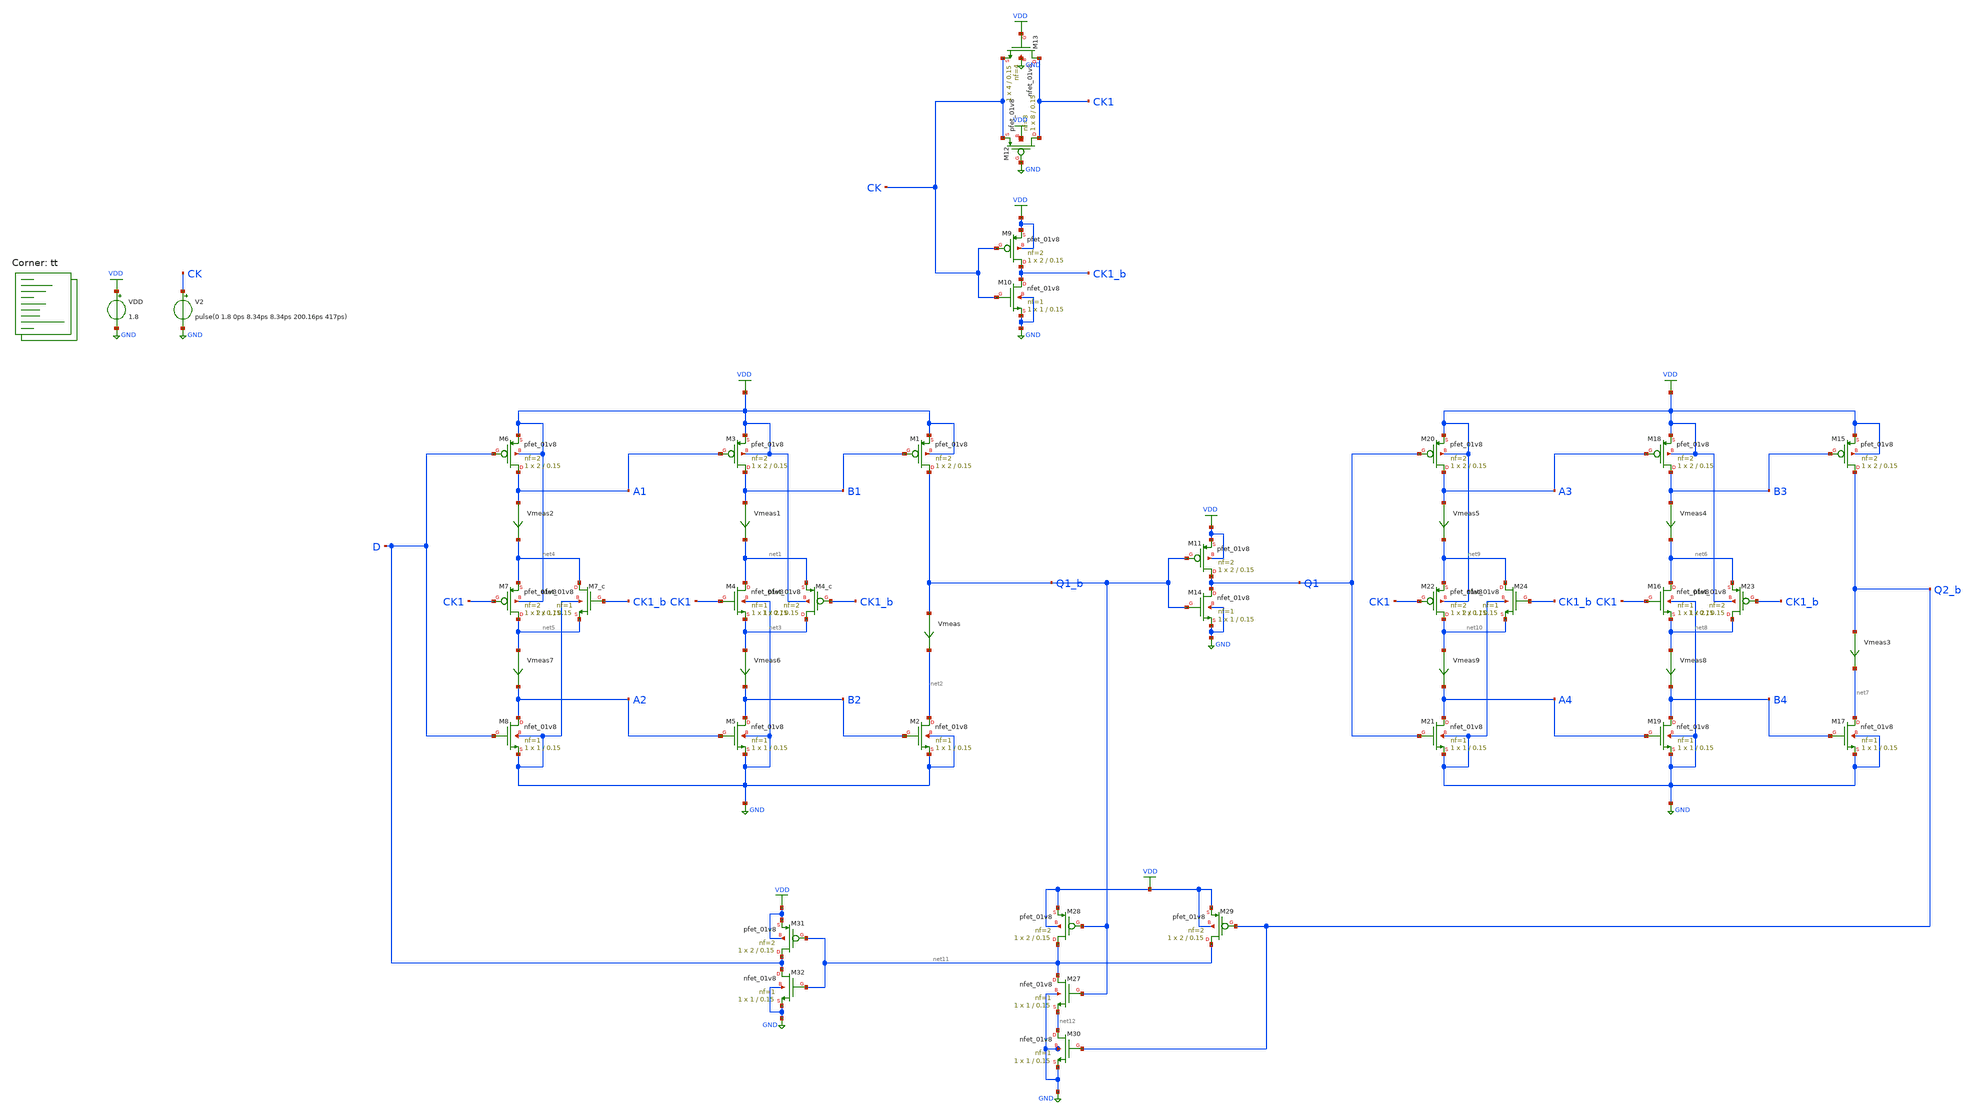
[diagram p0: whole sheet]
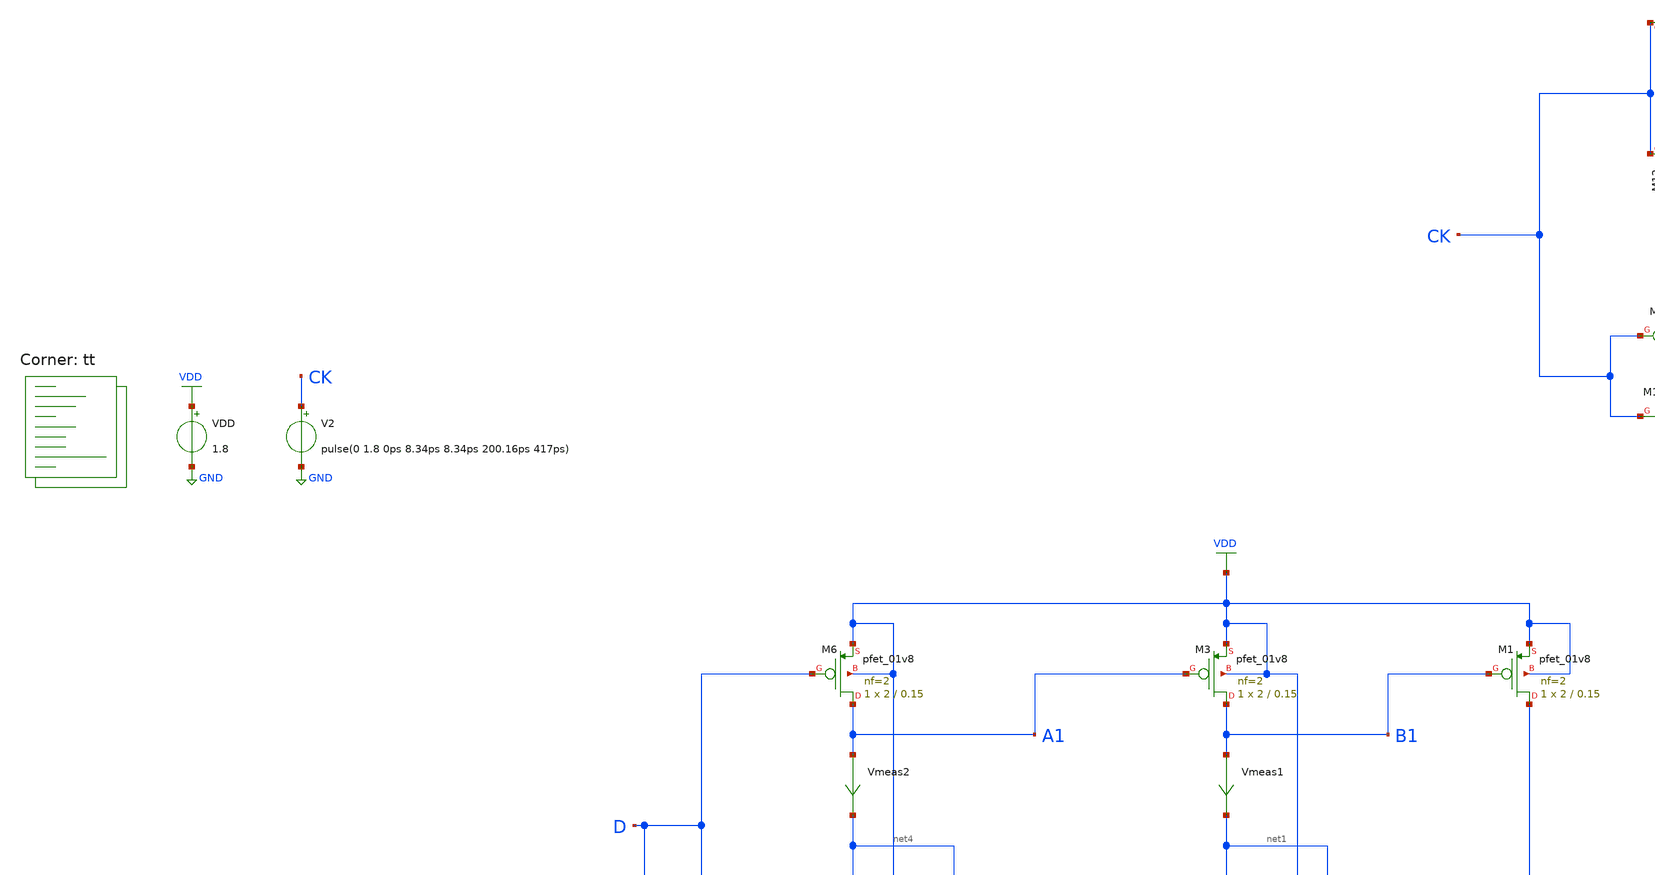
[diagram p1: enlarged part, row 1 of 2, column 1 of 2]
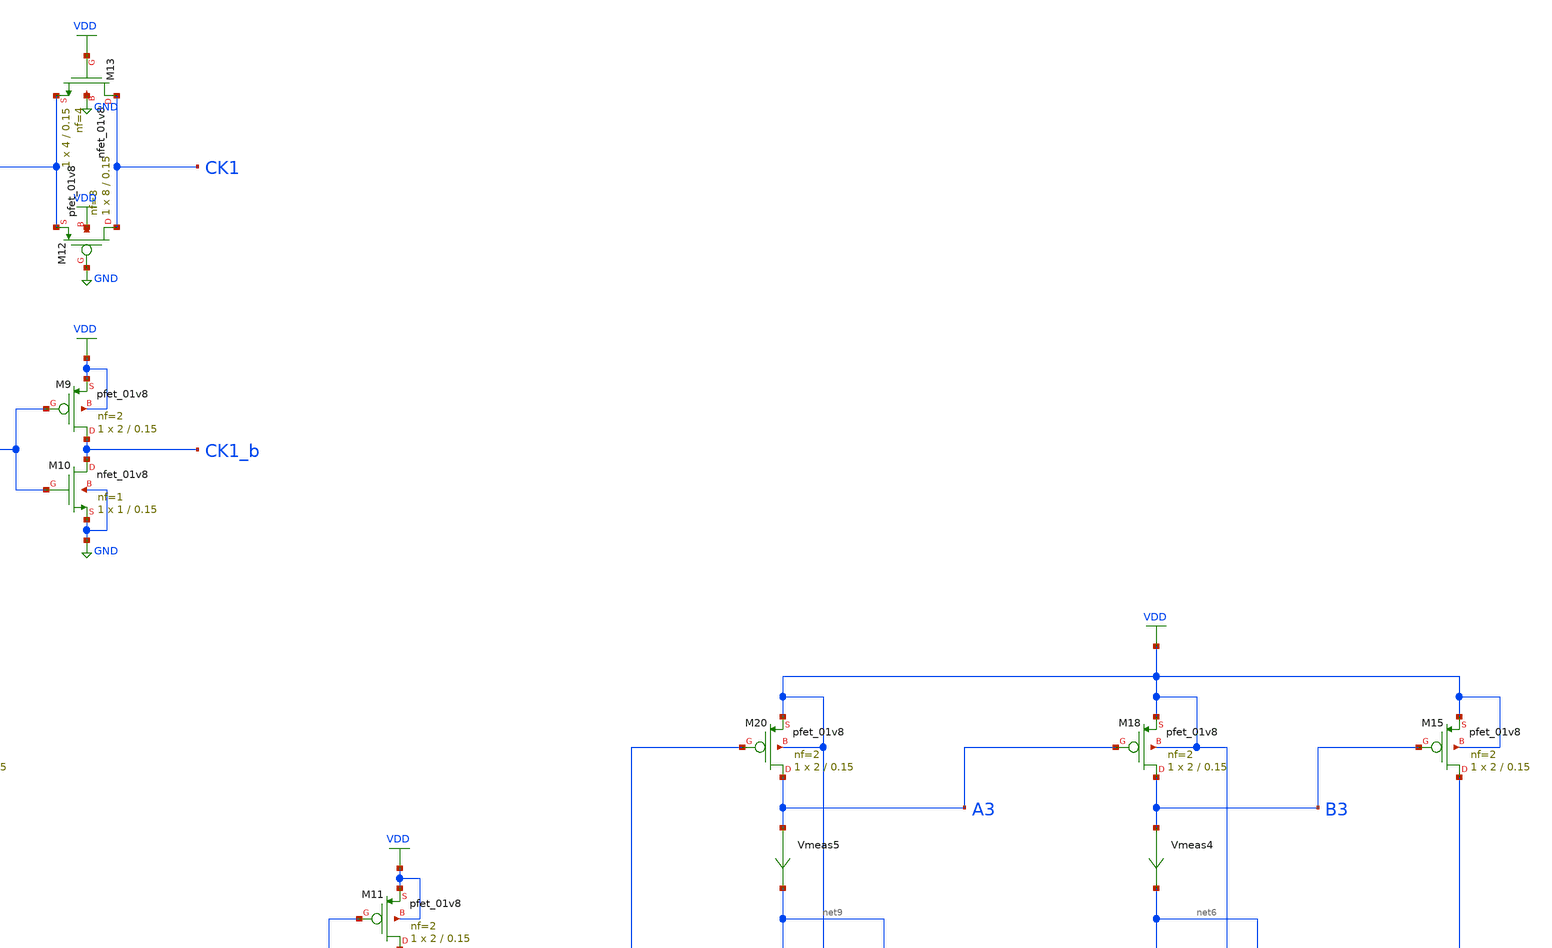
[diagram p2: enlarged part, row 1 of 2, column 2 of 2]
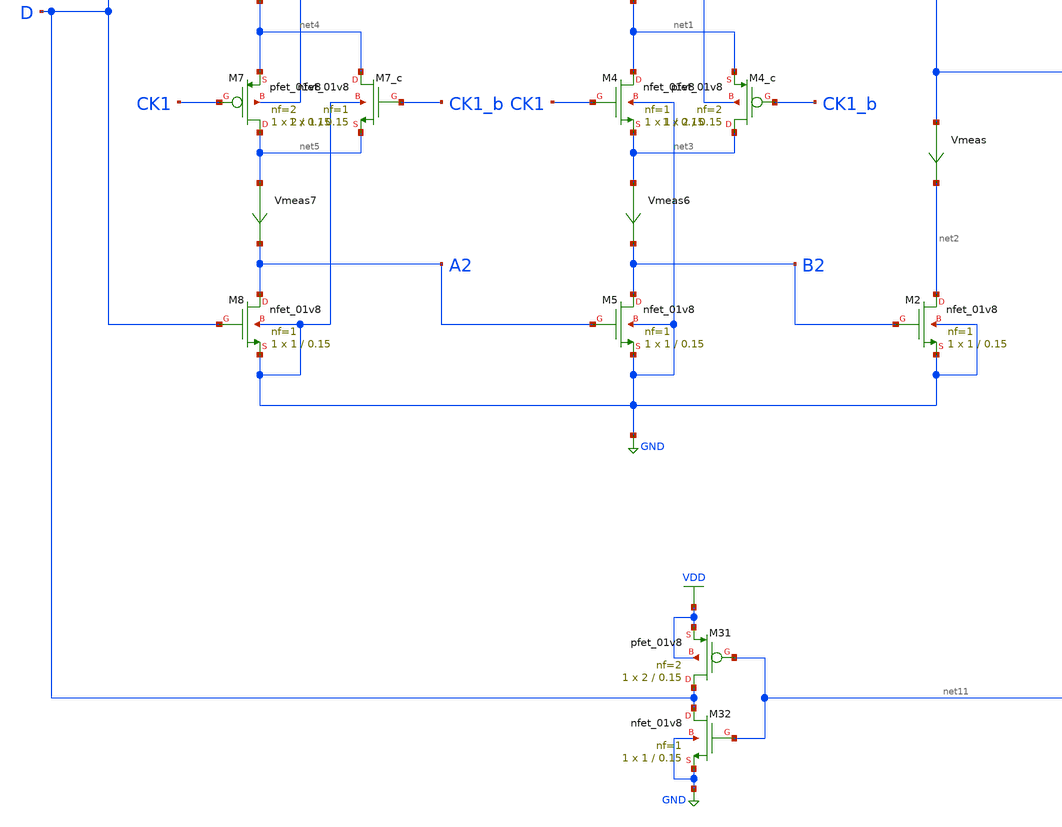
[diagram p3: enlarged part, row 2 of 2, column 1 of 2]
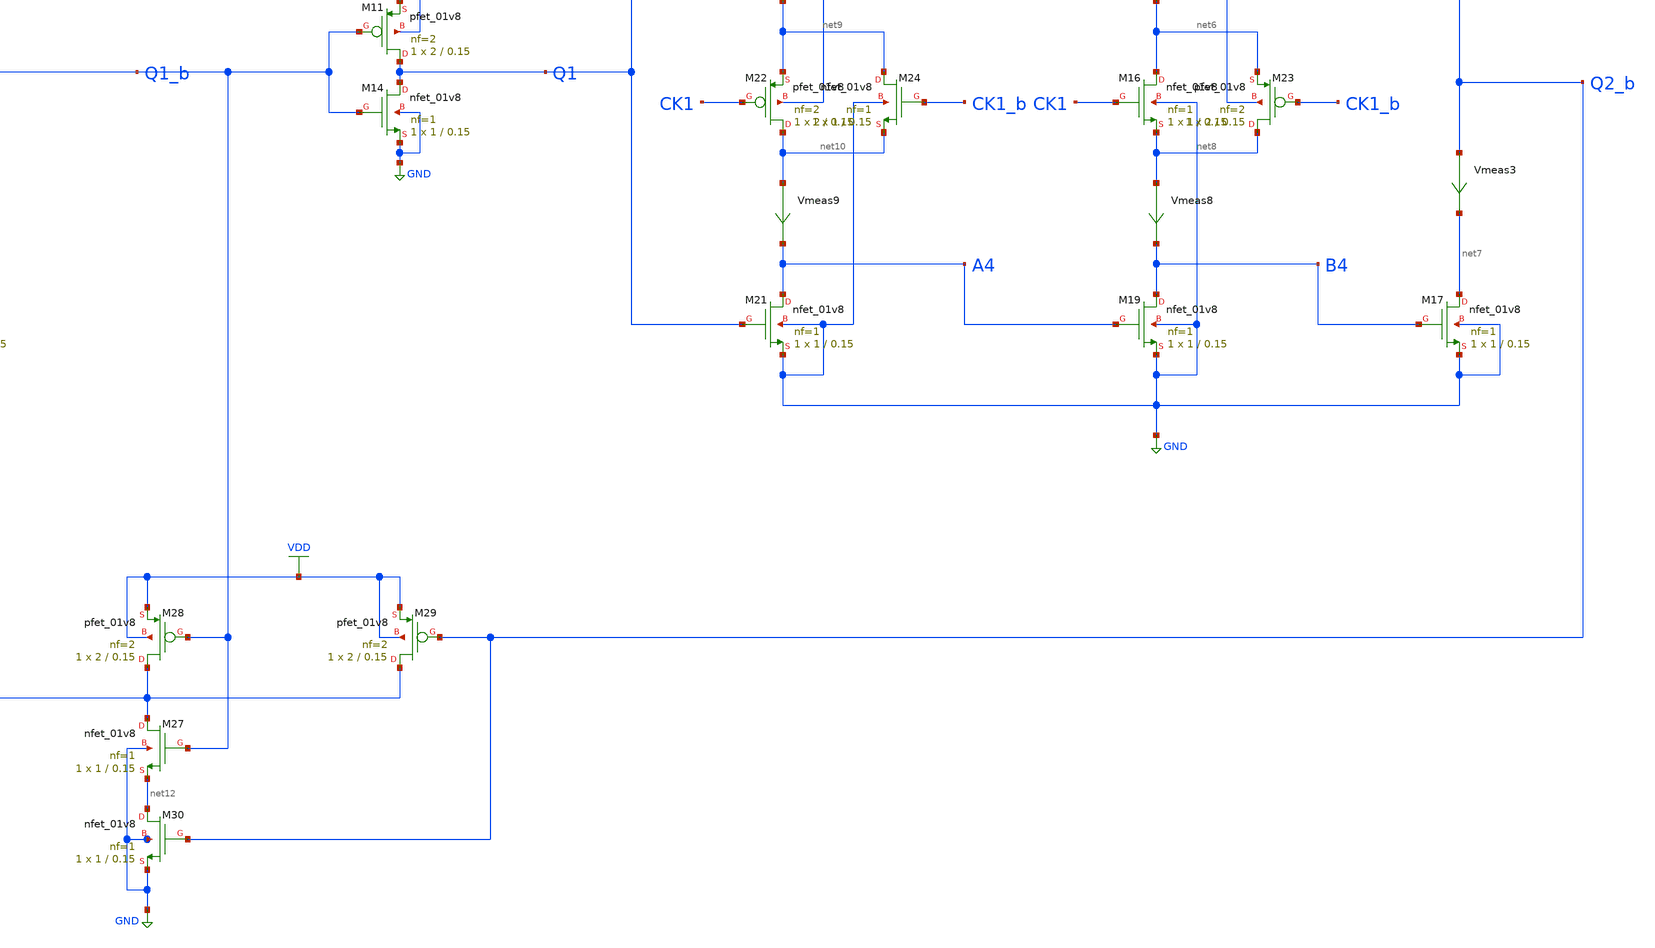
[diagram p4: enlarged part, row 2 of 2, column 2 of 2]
** sch_path: projects/pll/divider/xschem_ngspice/tb_TSPC_FF_comp_sw_divide3.sch
**.subckt tb_TSPC_FF_comp_sw_divide3
VDD VDD GND 1.8
XM1 Q1_b B1 VDD VDD sky130_fd_pr__pfet_01v8 L=0.15 W=2 nf=2 ad='int((nf+1)/2) * W/nf * 0.29' as='int((nf+2)/2) * W/nf * 0.29'
+ pd='2*int((nf+1)/2) * (W/nf + 0.29)' ps='2*int((nf+2)/2) * (W/nf + 0.29)' nrd='0.29 / W' nrs='0.29 / W'
+ sa=0 sb=0 sd=0 mult=1 m=1
XM4 net1 CK1 net3 GND sky130_fd_pr__nfet_01v8 L=0.15 W=1 nf=1 ad='int((nf+1)/2) * W/nf * 0.29' as='int((nf+2)/2) * W/nf * 0.29'
+ pd='2*int((nf+1)/2) * (W/nf + 0.29)' ps='2*int((nf+2)/2) * (W/nf + 0.29)' nrd='0.29 / W' nrs='0.29 / W'
+ sa=0 sb=0 sd=0 mult=1 m=1
Vmeas Q1_b net2 0
.save i(vmeas)
XM2 net2 B2 GND GND sky130_fd_pr__nfet_01v8 L=0.15 W=1 nf=1 ad='int((nf+1)/2) * W/nf * 0.29' as='int((nf+2)/2) * W/nf * 0.29'
+ pd='2*int((nf+1)/2) * (W/nf + 0.29)' ps='2*int((nf+2)/2) * (W/nf + 0.29)' nrd='0.29 / W' nrs='0.29 / W'
+ sa=0 sb=0 sd=0 mult=1 m=1
XM3 B1 A1 VDD VDD sky130_fd_pr__pfet_01v8 L=0.15 W=2 nf=2 ad='int((nf+1)/2) * W/nf * 0.29' as='int((nf+2)/2) * W/nf * 0.29'
+ pd='2*int((nf+1)/2) * (W/nf + 0.29)' ps='2*int((nf+2)/2) * (W/nf + 0.29)' nrd='0.29 / W' nrs='0.29 / W'
+ sa=0 sb=0 sd=0 mult=1 m=1
XM5 B2 A2 GND GND sky130_fd_pr__nfet_01v8 L=0.15 W=1 nf=1 ad='int((nf+1)/2) * W/nf * 0.29' as='int((nf+2)/2) * W/nf * 0.29'
+ pd='2*int((nf+1)/2) * (W/nf + 0.29)' ps='2*int((nf+2)/2) * (W/nf + 0.29)' nrd='0.29 / W' nrs='0.29 / W'
+ sa=0 sb=0 sd=0 mult=1 m=1
Vmeas1 B1 net1 0
.save i(vmeas1)
XM6 A1 D VDD VDD sky130_fd_pr__pfet_01v8 L=0.15 W=2 nf=2 ad='int((nf+1)/2) * W/nf * 0.29' as='int((nf+2)/2) * W/nf * 0.29'
+ pd='2*int((nf+1)/2) * (W/nf + 0.29)' ps='2*int((nf+2)/2) * (W/nf + 0.29)' nrd='0.29 / W' nrs='0.29 / W'
+ sa=0 sb=0 sd=0 mult=1 m=1
XM8 A2 D GND GND sky130_fd_pr__nfet_01v8 L=0.15 W=1 nf=1 ad='int((nf+1)/2) * W/nf * 0.29' as='int((nf+2)/2) * W/nf * 0.29'
+ pd='2*int((nf+1)/2) * (W/nf + 0.29)' ps='2*int((nf+2)/2) * (W/nf + 0.29)' nrd='0.29 / W' nrs='0.29 / W'
+ sa=0 sb=0 sd=0 mult=1 m=1
Vmeas2 A1 net4 0
.save i(vmeas2)
XM7 net5 CK1 net4 VDD sky130_fd_pr__pfet_01v8 L=0.15 W=2 nf=2 ad='int((nf+1)/2) * W/nf * 0.29' as='int((nf+2)/2) * W/nf * 0.29'
+ pd='2*int((nf+1)/2) * (W/nf + 0.29)' ps='2*int((nf+2)/2) * (W/nf + 0.29)' nrd='0.29 / W' nrs='0.29 / W'
+ sa=0 sb=0 sd=0 mult=1 m=1
XM4_c net3 CK1_b net1 VDD sky130_fd_pr__pfet_01v8 L=0.15 W=2 nf=2 ad='int((nf+1)/2) * W/nf * 0.29' as='int((nf+2)/2) * W/nf * 0.29'
+ pd='2*int((nf+1)/2) * (W/nf + 0.29)' ps='2*int((nf+2)/2) * (W/nf + 0.29)' nrd='0.29 / W' nrs='0.29 / W'
+ sa=0 sb=0 sd=0 mult=1 m=1
XM7_c net4 CK1_b net5 GND sky130_fd_pr__nfet_01v8 L=0.15 W=1 nf=1 ad='int((nf+1)/2) * W/nf * 0.29' as='int((nf+2)/2) * W/nf * 0.29'
+ pd='2*int((nf+1)/2) * (W/nf + 0.29)' ps='2*int((nf+2)/2) * (W/nf + 0.29)' nrd='0.29 / W' nrs='0.29 / W'
+ sa=0 sb=0 sd=0 mult=1 m=1
XM12 CK1 GND CK VDD sky130_fd_pr__pfet_01v8 L=0.15 W=8 nf=8 ad='int((nf+1)/2) * W/nf * 0.29' as='int((nf+2)/2) * W/nf * 0.29'
+ pd='2*int((nf+1)/2) * (W/nf + 0.29)' ps='2*int((nf+2)/2) * (W/nf + 0.29)' nrd='0.29 / W' nrs='0.29 / W'
+ sa=0 sb=0 sd=0 mult=1 m=1
XM13 CK1 VDD CK GND sky130_fd_pr__nfet_01v8 L=0.15 W=4 nf=4 ad='int((nf+1)/2) * W/nf * 0.29' as='int((nf+2)/2) * W/nf * 0.29'
+ pd='2*int((nf+1)/2) * (W/nf + 0.29)' ps='2*int((nf+2)/2) * (W/nf + 0.29)' nrd='0.29 / W' nrs='0.29 / W'
+ sa=0 sb=0 sd=0 mult=1 m=1
XM9 CK1_b CK VDD VDD sky130_fd_pr__pfet_01v8 L=0.15 W=2 nf=2 ad='int((nf+1)/2) * W/nf * 0.29' as='int((nf+2)/2) * W/nf * 0.29'
+ pd='2*int((nf+1)/2) * (W/nf + 0.29)' ps='2*int((nf+2)/2) * (W/nf + 0.29)' nrd='0.29 / W' nrs='0.29 / W'
+ sa=0 sb=0 sd=0 mult=1 m=1
XM10 CK1_b CK GND GND sky130_fd_pr__nfet_01v8 L=0.15 W=1 nf=1 ad='int((nf+1)/2) * W/nf * 0.29' as='int((nf+2)/2) * W/nf * 0.29'
+ pd='2*int((nf+1)/2) * (W/nf + 0.29)' ps='2*int((nf+2)/2) * (W/nf + 0.29)' nrd='0.29 / W' nrs='0.29 / W'
+ sa=0 sb=0 sd=0 mult=1 m=1
XM15 Q2_b B3 VDD VDD sky130_fd_pr__pfet_01v8 L=0.15 W=2 nf=2 ad='int((nf+1)/2) * W/nf * 0.29' as='int((nf+2)/2) * W/nf * 0.29'
+ pd='2*int((nf+1)/2) * (W/nf + 0.29)' ps='2*int((nf+2)/2) * (W/nf + 0.29)' nrd='0.29 / W' nrs='0.29 / W'
+ sa=0 sb=0 sd=0 mult=1 m=1
XM16 net6 CK1 net8 GND sky130_fd_pr__nfet_01v8 L=0.15 W=1 nf=1 ad='int((nf+1)/2) * W/nf * 0.29' as='int((nf+2)/2) * W/nf * 0.29'
+ pd='2*int((nf+1)/2) * (W/nf + 0.29)' ps='2*int((nf+2)/2) * (W/nf + 0.29)' nrd='0.29 / W' nrs='0.29 / W'
+ sa=0 sb=0 sd=0 mult=1 m=1
Vmeas3 Q2_b net7 0
.save i(vmeas3)
XM17 net7 B4 GND GND sky130_fd_pr__nfet_01v8 L=0.15 W=1 nf=1 ad='int((nf+1)/2) * W/nf * 0.29' as='int((nf+2)/2) * W/nf * 0.29'
+ pd='2*int((nf+1)/2) * (W/nf + 0.29)' ps='2*int((nf+2)/2) * (W/nf + 0.29)' nrd='0.29 / W' nrs='0.29 / W'
+ sa=0 sb=0 sd=0 mult=1 m=1
XM18 B3 A3 VDD VDD sky130_fd_pr__pfet_01v8 L=0.15 W=2 nf=2 ad='int((nf+1)/2) * W/nf * 0.29' as='int((nf+2)/2) * W/nf * 0.29'
+ pd='2*int((nf+1)/2) * (W/nf + 0.29)' ps='2*int((nf+2)/2) * (W/nf + 0.29)' nrd='0.29 / W' nrs='0.29 / W'
+ sa=0 sb=0 sd=0 mult=1 m=1
XM19 B4 A4 GND GND sky130_fd_pr__nfet_01v8 L=0.15 W=1 nf=1 ad='int((nf+1)/2) * W/nf * 0.29' as='int((nf+2)/2) * W/nf * 0.29'
+ pd='2*int((nf+1)/2) * (W/nf + 0.29)' ps='2*int((nf+2)/2) * (W/nf + 0.29)' nrd='0.29 / W' nrs='0.29 / W'
+ sa=0 sb=0 sd=0 mult=1 m=1
Vmeas4 B3 net6 0
.save i(vmeas4)
XM20 A3 Q1 VDD VDD sky130_fd_pr__pfet_01v8 L=0.15 W=2 nf=2 ad='int((nf+1)/2) * W/nf * 0.29' as='int((nf+2)/2) * W/nf * 0.29'
+ pd='2*int((nf+1)/2) * (W/nf + 0.29)' ps='2*int((nf+2)/2) * (W/nf + 0.29)' nrd='0.29 / W' nrs='0.29 / W'
+ sa=0 sb=0 sd=0 mult=1 m=1
XM21 A4 Q1 GND GND sky130_fd_pr__nfet_01v8 L=0.15 W=1 nf=1 ad='int((nf+1)/2) * W/nf * 0.29' as='int((nf+2)/2) * W/nf * 0.29'
+ pd='2*int((nf+1)/2) * (W/nf + 0.29)' ps='2*int((nf+2)/2) * (W/nf + 0.29)' nrd='0.29 / W' nrs='0.29 / W'
+ sa=0 sb=0 sd=0 mult=1 m=1
Vmeas5 A3 net9 0
.save i(vmeas5)
XM22 net10 CK1 net9 VDD sky130_fd_pr__pfet_01v8 L=0.15 W=2 nf=2 ad='int((nf+1)/2) * W/nf * 0.29' as='int((nf+2)/2) * W/nf * 0.29'
+ pd='2*int((nf+1)/2) * (W/nf + 0.29)' ps='2*int((nf+2)/2) * (W/nf + 0.29)' nrd='0.29 / W' nrs='0.29 / W'
+ sa=0 sb=0 sd=0 mult=1 m=1
XM23 net8 CK1_b net6 VDD sky130_fd_pr__pfet_01v8 L=0.15 W=2 nf=2 ad='int((nf+1)/2) * W/nf * 0.29' as='int((nf+2)/2) * W/nf * 0.29'
+ pd='2*int((nf+1)/2) * (W/nf + 0.29)' ps='2*int((nf+2)/2) * (W/nf + 0.29)' nrd='0.29 / W' nrs='0.29 / W'
+ sa=0 sb=0 sd=0 mult=1 m=1
XM24 net9 CK1_b net10 GND sky130_fd_pr__nfet_01v8 L=0.15 W=1 nf=1 ad='int((nf+1)/2) * W/nf * 0.29' as='int((nf+2)/2) * W/nf * 0.29'
+ pd='2*int((nf+1)/2) * (W/nf + 0.29)' ps='2*int((nf+2)/2) * (W/nf + 0.29)' nrd='0.29 / W' nrs='0.29 / W'
+ sa=0 sb=0 sd=0 mult=1 m=1
Vmeas6 net3 B2 0
.save i(vmeas6)
Vmeas7 net5 A2 0
.save i(vmeas7)
Vmeas8 net8 B4 0
.save i(vmeas8)
Vmeas9 net10 A4 0
.save i(vmeas9)
V2 CK GND pulse(0 1.8 0ps 8.34ps 8.34ps 200.16ps 417ps)
XM11 Q1 Q1_b VDD VDD sky130_fd_pr__pfet_01v8 L=0.15 W=2 nf=2 ad='int((nf+1)/2) * W/nf * 0.29' as='int((nf+2)/2) * W/nf * 0.29'
+ pd='2*int((nf+1)/2) * (W/nf + 0.29)' ps='2*int((nf+2)/2) * (W/nf + 0.29)' nrd='0.29 / W' nrs='0.29 / W'
+ sa=0 sb=0 sd=0 mult=1 m=1
XM14 Q1 Q1_b GND GND sky130_fd_pr__nfet_01v8 L=0.15 W=1 nf=1 ad='int((nf+1)/2) * W/nf * 0.29' as='int((nf+2)/2) * W/nf * 0.29'
+ pd='2*int((nf+1)/2) * (W/nf + 0.29)' ps='2*int((nf+2)/2) * (W/nf + 0.29)' nrd='0.29 / W' nrs='0.29 / W'
+ sa=0 sb=0 sd=0 mult=1 m=1
XM27 net11 Q1_b net12 GND sky130_fd_pr__nfet_01v8 L=0.15 W=1 nf=1 ad='int((nf+1)/2) * W/nf * 0.29' as='int((nf+2)/2) * W/nf * 0.29'
+ pd='2*int((nf+1)/2) * (W/nf + 0.29)' ps='2*int((nf+2)/2) * (W/nf + 0.29)' nrd='0.29 / W' nrs='0.29 / W'
+ sa=0 sb=0 sd=0 mult=1 m=1
XM28 net11 Q1_b VDD VDD sky130_fd_pr__pfet_01v8 L=0.15 W=2 nf=2 ad='int((nf+1)/2) * W/nf * 0.29' as='int((nf+2)/2) * W/nf * 0.29'
+ pd='2*int((nf+1)/2) * (W/nf + 0.29)' ps='2*int((nf+2)/2) * (W/nf + 0.29)' nrd='0.29 / W' nrs='0.29 / W'
+ sa=0 sb=0 sd=0 mult=1 m=1
XM29 net11 Q2_b VDD VDD sky130_fd_pr__pfet_01v8 L=0.15 W=2 nf=2 ad='int((nf+1)/2) * W/nf * 0.29' as='int((nf+2)/2) * W/nf * 0.29'
+ pd='2*int((nf+1)/2) * (W/nf + 0.29)' ps='2*int((nf+2)/2) * (W/nf + 0.29)' nrd='0.29 / W' nrs='0.29 / W'
+ sa=0 sb=0 sd=0 mult=1 m=1
XM30 net12 Q2_b GND GND sky130_fd_pr__nfet_01v8 L=0.15 W=1 nf=1 ad='int((nf+1)/2) * W/nf * 0.29' as='int((nf+2)/2) * W/nf * 0.29'
+ pd='2*int((nf+1)/2) * (W/nf + 0.29)' ps='2*int((nf+2)/2) * (W/nf + 0.29)' nrd='0.29 / W' nrs='0.29 / W'
+ sa=0 sb=0 sd=0 mult=1 m=1
XM31 D net11 VDD VDD sky130_fd_pr__pfet_01v8 L=0.15 W=2 nf=2 ad='int((nf+1)/2) * W/nf * 0.29' as='int((nf+2)/2) * W/nf * 0.29'
+ pd='2*int((nf+1)/2) * (W/nf + 0.29)' ps='2*int((nf+2)/2) * (W/nf + 0.29)' nrd='0.29 / W' nrs='0.29 / W'
+ sa=0 sb=0 sd=0 mult=1 m=1
XM32 D net11 GND GND sky130_fd_pr__nfet_01v8 L=0.15 W=1 nf=1 ad='int((nf+1)/2) * W/nf * 0.29' as='int((nf+2)/2) * W/nf * 0.29'
+ pd='2*int((nf+1)/2) * (W/nf + 0.29)' ps='2*int((nf+2)/2) * (W/nf + 0.29)' nrd='0.29 / W' nrs='0.29 / W'
+ sa=0 sb=0 sd=0 mult=1 m=1
**** begin user architecture code



.include /foss/pdks/sky130A/libs.ref/sky130_fd_sc_hd/spice/sky130_fd_sc_hd.spice

.option method=gear
.option wnflag=1
.option savecurrents

.save @m.xm1.msky130_fd_pr__pfet_01v8[gm] @m.xm2.msky130_fd_pr__nfet_01v8[gm] @m.xm3.msky130_fd_pr__pfet_01v8[gm] @m.xm4.msky130_fd_pr__nfet_01v8[gm] @m.xm4_c.msky130_fd_pr__pfet_01v8[gm] @m.xm5.msky130_fd_pr__nfet_01v8[gm] @m.xm6.msky130_fd_pr__pfet_01v8[gm] @m.xm7.msky130_fd_pr__pfet_01v8[gm] @m.xm7_c.msky130_fd_pr__nfet_01v8[gm] @m.xm8.msky130_fd_pr__nfet_01v8[gm]

*.ic v(d)=0
*.ic v(q)=0
*.ic v(q1)=0

.control

  save v(d) v(q1) v(q2) v(q1_b) v(q2_b) v(q3) v(a1) v(a2) v(a3) v(a4) v(b1) v(b2) v(b3) v(b4) v(ck)
+ v(ck1) v(ck1_b)
  * save all
  * tran 0.1n 1u
  tran 1p 20n

  remzerovec
  write tb_TSPC_FF_comp_sw_divide3.raw
  * set appendwrite

.endc



.lib $::SKYWATER_MODELS/sky130.lib.spice tt
**** end user architecture code
**.ends
.GLOBAL GND
.GLOBAL VDD
.end
